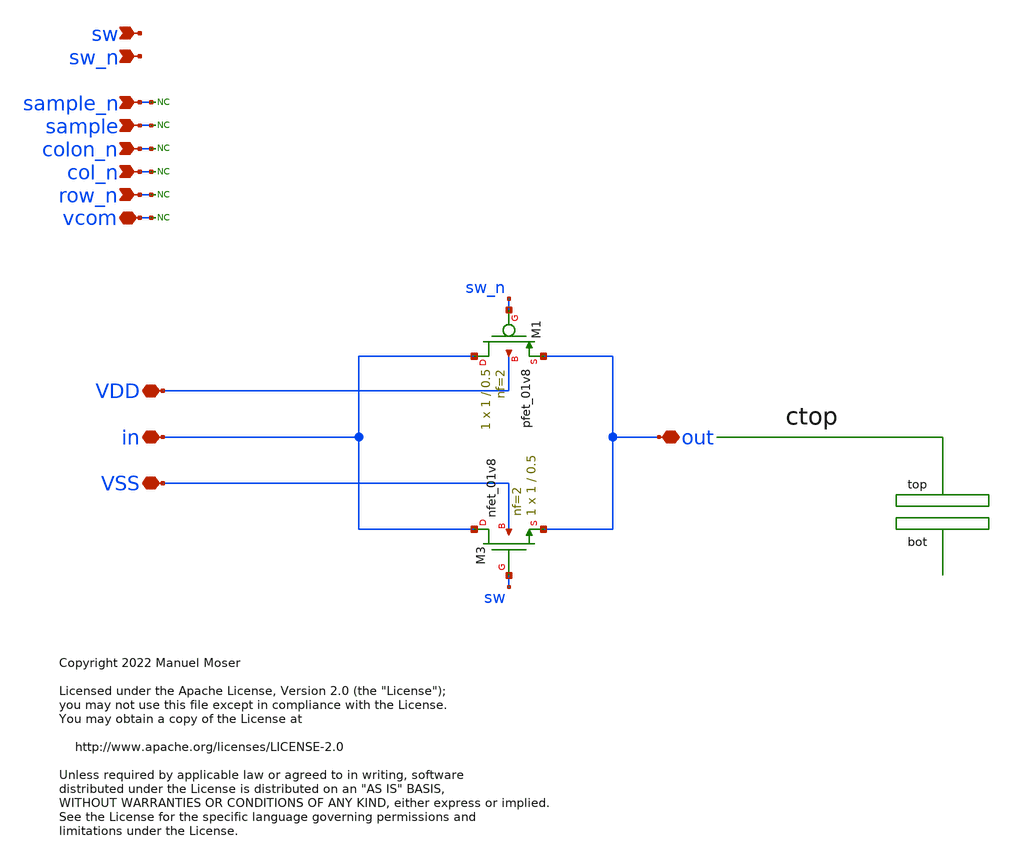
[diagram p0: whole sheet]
** sch_path: xschem/adc_array_circuit_gate.sch
* Copyright 2022 Manuel Moser
* Licensed under the Apache License, Version 2.0 (the "License");
**.subckt adc_array_circuit_gate sw sw_n vcom row_n col_n colon_n VDD VSS sample sample_n in out
*.ipin sw
*.ipin sw_n
*.iopin vcom
*.ipin row_n
*.ipin col_n
*.ipin colon_n
*.iopin VDD
*.iopin VSS
*.ipin sample
*.ipin sample_n
*.iopin in
*.iopin out
* noconn row_n
* noconn col_n
* noconn colon_n
* noconn vcom
* noconn sample
* noconn sample_n
XM1 in sw_n out VDD sky130_fd_pr__pfet_01v8 L=0.5 W=1 nf=2 ad='int((nf+1)/2) * W/nf * 0.29' as='int((nf+2)/2) * W/nf * 0.29'
+ pd='2*int((nf+1)/2) * (W/nf + 0.29)' ps='2*int((nf+2)/2) * (W/nf + 0.29)' nrd='0.29 / W' nrs='0.29 / W'
+ sa=0 sb=0 sd=0 mult=1 m=1
XM3 in sw out VSS sky130_fd_pr__nfet_01v8 L=0.5 W=1 nf=2 ad='int((nf+1)/2) * W/nf * 0.29' as='int((nf+2)/2) * W/nf * 0.29'
+ pd='2*int((nf+1)/2) * (W/nf + 0.29)' ps='2*int((nf+2)/2) * (W/nf + 0.29)' nrd='0.29 / W' nrs='0.29 / W'
+ sa=0 sb=0 sd=0 mult=1 m=1
**.ends
.end
